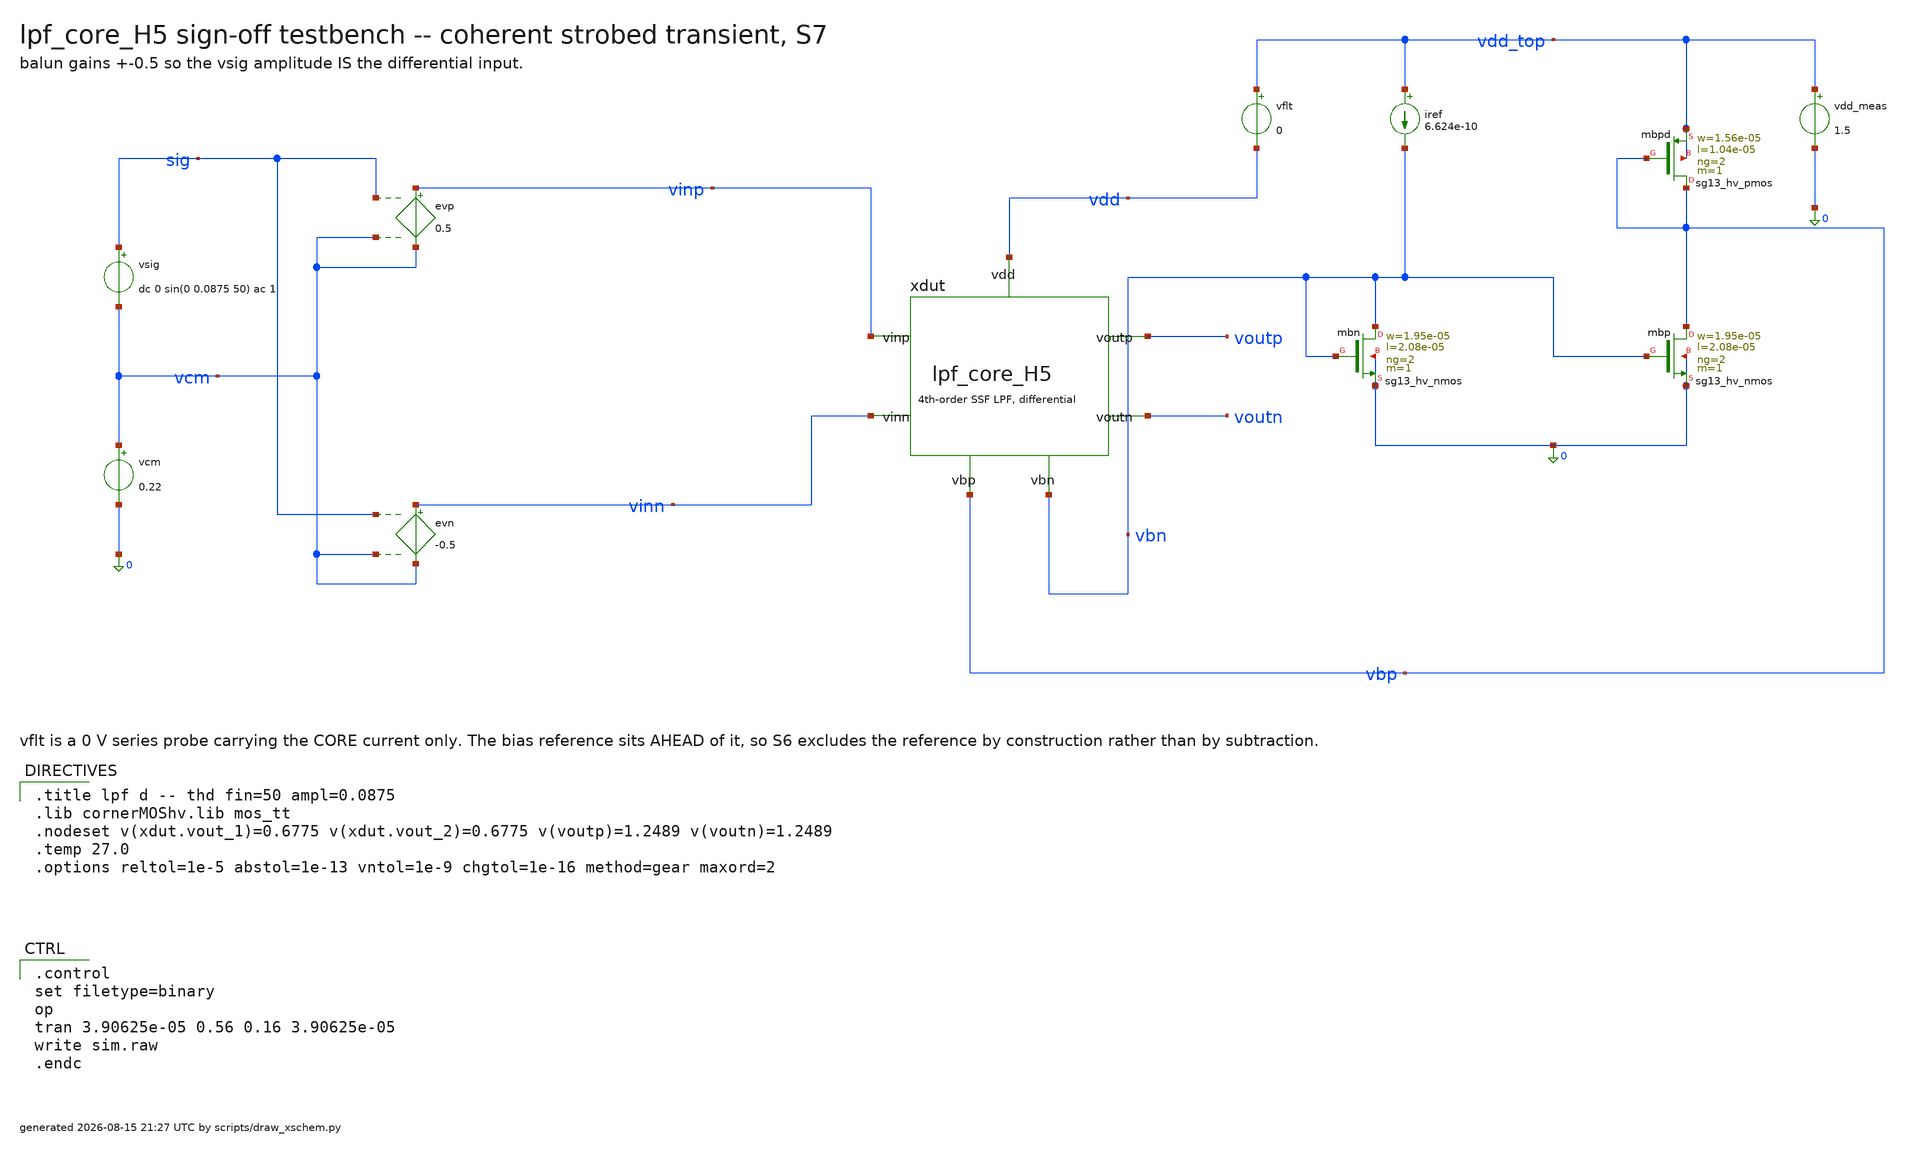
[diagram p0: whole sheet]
** sch_path: signoff/post-pvt/H5-lean/lpf_tb_H5_thd.sch
**.subckt lpf_tb_H5_thd
vsig sig vcm dc 0 sin(0 0.0875 50) ac 1
vcm vcm 0 0.22
evp vinp vcm sig vcm 0.5
evn vinn vcm sig vcm -0.5
xdut vinp vinn voutp voutn vbn vbp vdd lpf_core_H5
vflt vdd_top vdd 0
vdd_meas vdd_top 0 1.5
iref vdd_top vbn 6.624e-10
Xmbn vbn vbn 0 0 sg13_hv_nmos w=1.95e-05 l=2.08e-05 ng=2 m=1 mm_ok=1
Xmbp vbp vbn 0 0 sg13_hv_nmos w=1.95e-05 l=2.08e-05 ng=2 m=1 mm_ok=1
Xmbpd vbp vbp vdd_top vdd_top sg13_hv_pmos w=1.56e-05 l=1.04e-05 ng=2 m=1 mm_ok=1
**** begin user architecture code

.title lpf d -- thd fin=50 ampl=0.0875
.lib cornerMOShv.lib mos_tt
.nodeset v(xdut.vout_1)=0.6775 v(xdut.vout_2)=0.6775 v(voutp)=1.2489 v(voutn)=1.2489
.temp 27.0
.options reltol=1e-5 abstol=1e-13 vntol=1e-9 chgtol=1e-16 method=gear maxord=2


.control
set filetype=binary
op
tran 3.90625e-05 0.56 0.16 3.90625e-05
write sim.raw
.endc

**** end user architecture code
**.ends

* expanding   symbol:  lpf_core_H5.sym # of pins=7
** sym_path: signoff/post-pvt/H5-lean/lpf_core_H5.sym
** sch_path: signoff/post-pvt/H5-lean/lpf_core_H5.sch
.subckt lpf_core_H5 vinp vinn voutp voutn vbn vbp vdd
*.ipin vinp
*.ipin vinn
*.opin voutp
*.opin voutn
*.ipin vdd
*.ipin vbn
*.ipin vbp
Xm2 net2 vinp vout_1 vout_1 sg13_hv_pmos w=1.56e-05 l=1.04e-05 ng=2 m=1 mm_ok=1
Xm5 net3 vinn vout_2 vout_2 sg13_hv_pmos w=1.56e-05 l=1.04e-05 ng=2 m=1 mm_ok=1
Xm4 vout_1 net2 0 0 sg13_hv_nmos w=1.5e-06 l=4.5e-05 ng=1 m=1 mm_ok=1
Xm8 vout_2 net3 0 0 sg13_hv_nmos w=1.5e-06 l=4.5e-05 ng=1 m=1 mm_ok=1
Xm9 net2 vbn 0 0 sg13_hv_nmos w=1.95e-05 l=2.08e-05 ng=2 m=1 mm_ok=1
Xm10 net3 vbn 0 0 sg13_hv_nmos w=1.95e-05 l=2.08e-05 ng=2 m=1 mm_ok=1
Xmst vout_1 vbr net4 net4 sg13_hv_pmos w=3.24e-06 l=2.184e-05 ng=1 m=1 mm_ok=1
Xmstn vout_2 vbr net1 net1 sg13_hv_pmos w=3.24e-06 l=2.184e-05 ng=1 m=1 mm_ok=1
Xm0 net4 vout_1 voutp voutp sg13_hv_pmos w=4e-06 l=1.5e-05 ng=1 m=1 mm_ok=1
Xm1 net1 vout_2 voutn voutn sg13_hv_pmos w=4e-06 l=1.5e-05 ng=1 m=1 mm_ok=1
Xm14 voutp net4 vdd vdd sg13_hv_pmos w=8.5e-06 l=2.2e-05 ng=1 m=1 mm_ok=1
Xm15 voutn net1 vdd vdd sg13_hv_pmos w=8.5e-06 l=2.2e-05 ng=1 m=1 mm_ok=1
Xr1 rep_x rep_x vdd vdd sg13_hv_pmos w=8.5e-06 l=2.2e-05 ng=1 m=1 mm_ok=1
Xr2 vbr vbr rep_x rep_x sg13_hv_pmos w=3.24e-06 l=2.184e-05 ng=1 m=1 mm_ok=1
Xr3 vbr vbn 0 0 sg13_hv_nmos w=1.95e-05 l=2.08e-05 ng=2 m=3 mm_ok=1
c13 net2 vout_1 5.06142e-12 m=1
c17 net3 vout_2 5.06142e-12 m=1
c19 vout_2 vout_1 2.02884e-11 m=1
c1 voutp net4 4.66887e-11 m=1
c10 voutn net1 4.66887e-11 m=1
c12 voutn voutp 1.6618e-11 m=1
.ends

.end
